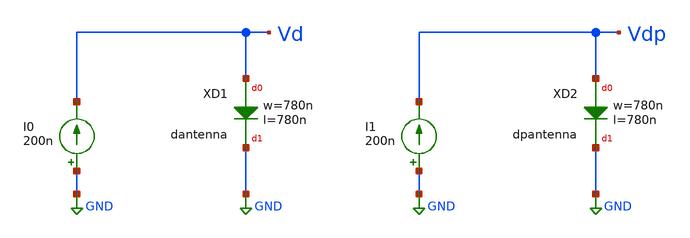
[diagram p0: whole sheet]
** sch_path: ihp-sg13g2/xschem_libs/sg13g2_tests_ase/dc_diode_temp/schematic/dc_diode_temp.sch
* Copyright 2023 IHP PDK Authors
**.subckt dc_diode_temp
XXD1 Vd GND dantenna l=780n w=780n
I0 GND Vd 200n
I1 GND Vdp 200n
XXD2 Vdp GND dpantenna l=780n w=780n
**.ends
.GLOBAL GND
.end
